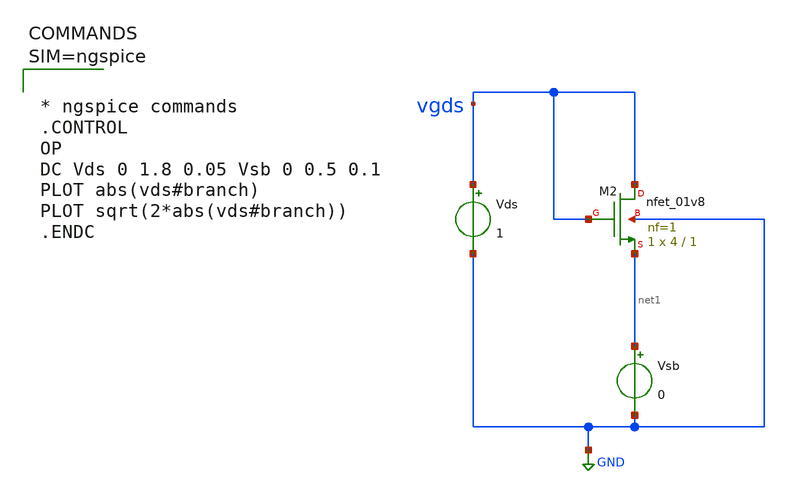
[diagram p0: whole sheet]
** sch_path: work/xschem/param_extract2.sch
**.subckt param_extract2
Vds vgds GND 1
Vsb net1 GND 0
XM2 vgds vgds net1 GND sky130_fd_pr__nfet_01v8 L=1 W=4 nf=1 ad='int((1 + 1)/2) * 4 / 1 * 0.29' as='int((1 + 2)/2) * 4 / 1 * 0.29'
+ pd='2*int((1 + 1)/2) * (4 / 1 + 0.29)' ps='2*int((1 + 2)/2) * (4 / 1 + 0.29)' nrd='0.29 / 4 ' nrs='0.29 / 4 '
+ sa=0 sb=0 sd=0 mult=1 m=1
**** begin user architecture code



* ngspice commands
.CONTROL
OP
DC Vds 0 1.8 0.05 Vsb 0 0.5 0.1
PLOT abs(vds#branch)
PLOT sqrt(2*abs(vds#branch))
.ENDC





** opencircuitdesign pdks install
.lib $::SKYWATER_MODELS/sky130.lib.spice tt

**** end user architecture code
**.ends
.GLOBAL GND
.end
